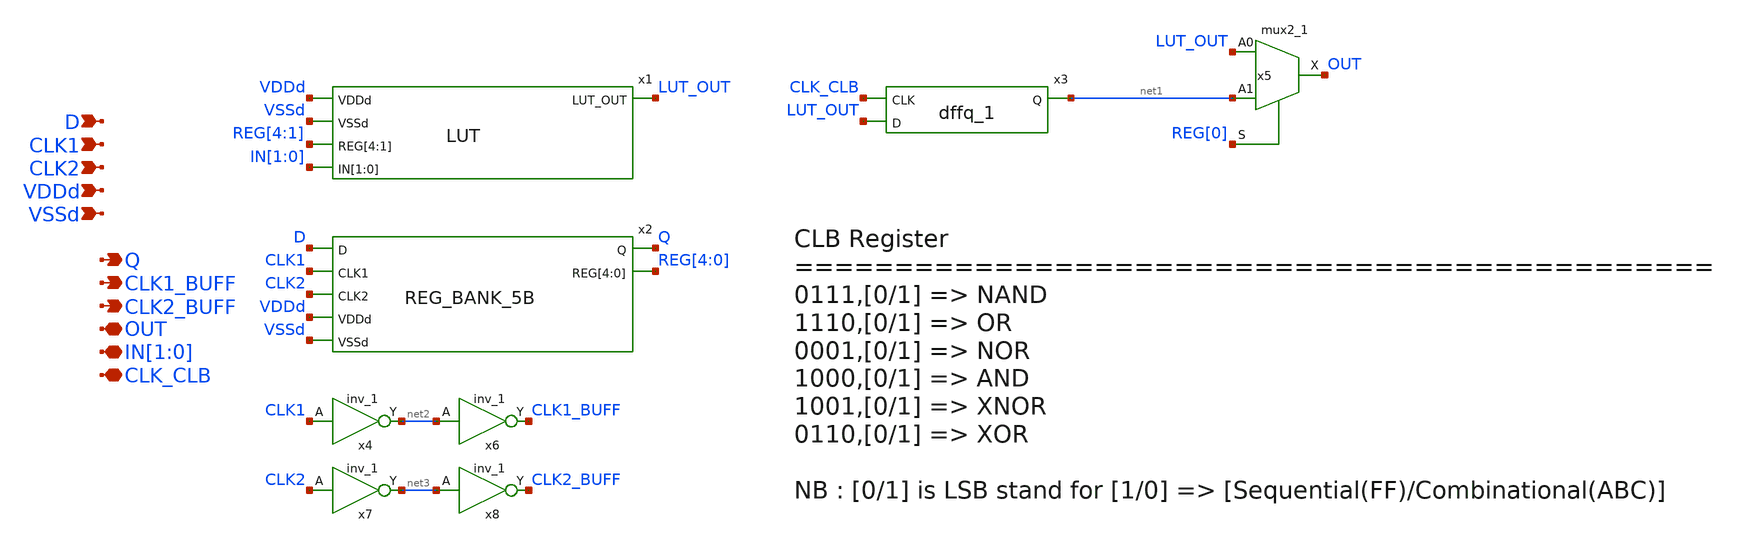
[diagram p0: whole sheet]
** sch_path: designs/libs/core_fpga/clb_2bit/clb_2bit_sc.sch
**.subckt clb_2bit_sc VDDd VSSd D CLK1 CLK2 Q OUT IN[1],IN[0] CLK_CLB CLK1_BUFF CLK2_BUFF
*.ipin VDDd
*.ipin VSSd
*.ipin D
*.ipin CLK1
*.ipin CLK2
*.opin Q
*.iopin OUT
*.iopin IN[1],IN[0]
*.iopin CLK_CLB
*.opin CLK1_BUFF
*.opin CLK2_BUFF
x3 CLK_CLB LUT_OUT VDD VNW VPW VSS gf180mcu_fd_sc_mcu9t5v0__dffq_1
x5 LUT_OUT net1 REG[0] VSSd VDDd VSSd VDDd OUT gf180mcu_fd_sc_mcu9t5v0__mux2_1
x1 VDDd VSSd REG[4] REG[3] REG[2] REG[1] IN[1] IN[0] LUT_OUT LUT
x2 D CLK1 CLK2 VDDd VSSd Q REG[4] REG[3] REG[2] REG[1] REG[0] REG_BANK_5B
x4 CLK1 VSSd VDDd VSSd VDDd net2 gf180mcu_fd_sc_mcu9t5v0__inv_1
x6 net2 VSSd VDDd VSSd VDDd CLK1_BUFF gf180mcu_fd_sc_mcu9t5v0__inv_1
x7 CLK2 VSSd VDDd VSSd VDDd net3 gf180mcu_fd_sc_mcu9t5v0__inv_1
x8 net3 VSSd VDDd VSSd VDDd CLK2_BUFF gf180mcu_fd_sc_mcu9t5v0__inv_1
**.ends
.end
